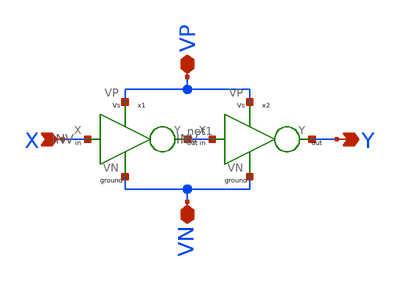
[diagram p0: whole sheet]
** sch_path: Blocks/Buffer/Buff.sch
**.subckt Buff X Y VN VP
*.ipin X
*.opin Y
*.iopin VN
*.iopin VP
x1 X net1 VP VN INV
x2 net1 Y VP VN INV
**.ends

* expanding   symbol:  Pico_project/INV/INV.sym # of pins=4
** sym_path: component/INV/INV.sym
** sch_path: component/INV/INV.sch
.subckt INV X Y VP VN
*.ipin X
*.opin Y
*.iopin VN
*.iopin VP
XM1 Y X VN VN sky130_fd_pr__nfet_01v8 L=0.15 W=0.42 nf=1 ad='int((nf+1)/2) * W/nf * 0.29' as='int((nf+2)/2) * W/nf * 0.29'
+ pd='2*int((nf+1)/2) * (W/nf + 0.29)' ps='2*int((nf+2)/2) * (W/nf + 0.29)' nrd='0.29 / W' nrs='0.29 / W'
+ sa=0 sb=0 sd=0 mult=1 m=1
XM2 Y X VP VP sky130_fd_pr__pfet_01v8 L=0.15 W=1.26 nf=1 ad='int((nf+1)/2) * W/nf * 0.29' as='int((nf+2)/2) * W/nf * 0.29'
+ pd='2*int((nf+1)/2) * (W/nf + 0.29)' ps='2*int((nf+2)/2) * (W/nf + 0.29)' nrd='0.29 / W' nrs='0.29 / W'
+ sa=0 sb=0 sd=0 mult=1 m=1
.ends

.end
